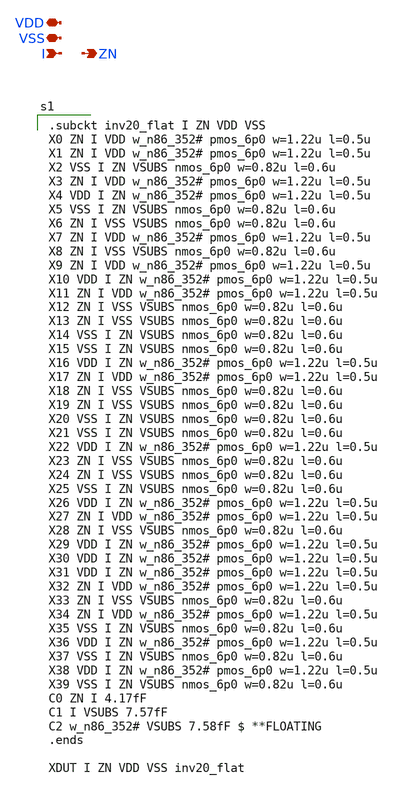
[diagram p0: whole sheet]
** sch_path: xschem/inv20_PEX.sch
**.subckt inv20_PEX VDD VSS I ZN
*.iopin VDD
*.iopin VSS
*.ipin I
*.opin ZN
**** begin user architecture code

.subckt inv20_flat I ZN VDD VSS
X0 ZN I VDD w_n86_352# pmos_6p0 w=1.22u l=0.5u
X1 ZN I VDD w_n86_352# pmos_6p0 w=1.22u l=0.5u
X2 VSS I ZN VSUBS nmos_6p0 w=0.82u l=0.6u
X3 ZN I VDD w_n86_352# pmos_6p0 w=1.22u l=0.5u
X4 VDD I ZN w_n86_352# pmos_6p0 w=1.22u l=0.5u
X5 VSS I ZN VSUBS nmos_6p0 w=0.82u l=0.6u
X6 ZN I VSS VSUBS nmos_6p0 w=0.82u l=0.6u
X7 ZN I VDD w_n86_352# pmos_6p0 w=1.22u l=0.5u
X8 ZN I VSS VSUBS nmos_6p0 w=0.82u l=0.6u
X9 ZN I VDD w_n86_352# pmos_6p0 w=1.22u l=0.5u
X10 VDD I ZN w_n86_352# pmos_6p0 w=1.22u l=0.5u
X11 ZN I VDD w_n86_352# pmos_6p0 w=1.22u l=0.5u
X12 ZN I VSS VSUBS nmos_6p0 w=0.82u l=0.6u
X13 ZN I VSS VSUBS nmos_6p0 w=0.82u l=0.6u
X14 VSS I ZN VSUBS nmos_6p0 w=0.82u l=0.6u
X15 VSS I ZN VSUBS nmos_6p0 w=0.82u l=0.6u
X16 VDD I ZN w_n86_352# pmos_6p0 w=1.22u l=0.5u
X17 ZN I VDD w_n86_352# pmos_6p0 w=1.22u l=0.5u
X18 ZN I VSS VSUBS nmos_6p0 w=0.82u l=0.6u
X19 ZN I VSS VSUBS nmos_6p0 w=0.82u l=0.6u
X20 VSS I ZN VSUBS nmos_6p0 w=0.82u l=0.6u
X21 VSS I ZN VSUBS nmos_6p0 w=0.82u l=0.6u
X22 VDD I ZN w_n86_352# pmos_6p0 w=1.22u l=0.5u
X23 ZN I VSS VSUBS nmos_6p0 w=0.82u l=0.6u
X24 ZN I VSS VSUBS nmos_6p0 w=0.82u l=0.6u
X25 VSS I ZN VSUBS nmos_6p0 w=0.82u l=0.6u
X26 VDD I ZN w_n86_352# pmos_6p0 w=1.22u l=0.5u
X27 ZN I VDD w_n86_352# pmos_6p0 w=1.22u l=0.5u
X28 ZN I VSS VSUBS nmos_6p0 w=0.82u l=0.6u
X29 VDD I ZN w_n86_352# pmos_6p0 w=1.22u l=0.5u
X30 VDD I ZN w_n86_352# pmos_6p0 w=1.22u l=0.5u
X31 VDD I ZN w_n86_352# pmos_6p0 w=1.22u l=0.5u
X32 ZN I VDD w_n86_352# pmos_6p0 w=1.22u l=0.5u
X33 ZN I VSS VSUBS nmos_6p0 w=0.82u l=0.6u
X34 ZN I VDD w_n86_352# pmos_6p0 w=1.22u l=0.5u
X35 VSS I ZN VSUBS nmos_6p0 w=0.82u l=0.6u
X36 VDD I ZN w_n86_352# pmos_6p0 w=1.22u l=0.5u
X37 VSS I ZN VSUBS nmos_6p0 w=0.82u l=0.6u
X38 VDD I ZN w_n86_352# pmos_6p0 w=1.22u l=0.5u
X39 VSS I ZN VSUBS nmos_6p0 w=0.82u l=0.6u
C0 ZN I 4.17fF
C1 I VSUBS 7.57fF
C2 w_n86_352# VSUBS 7.58fF $ **FLOATING
.ends

XDUT I ZN VDD VSS inv20_flat


**** end user architecture code
**.ends
.end
